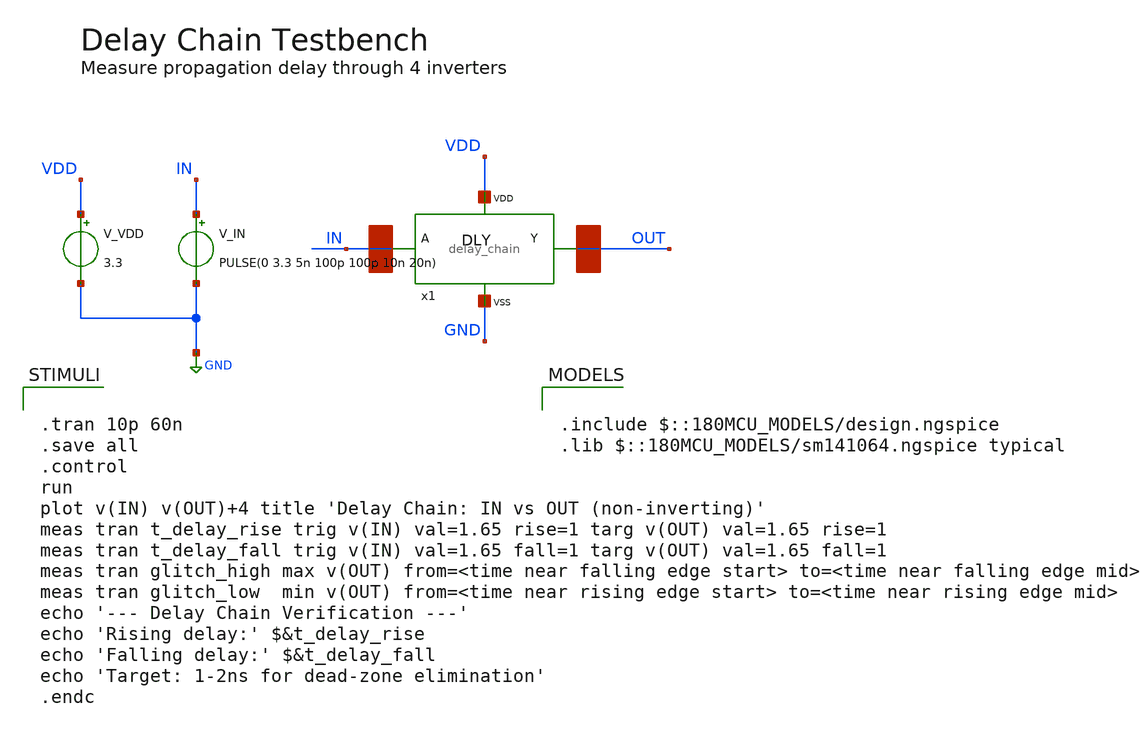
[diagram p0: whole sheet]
** sch_path: designs/libs/PDF/delay_chain_tb.sch
**.subckt delay_chain_tb
x1 IN OUT VDD GND delay_chain
V_IN IN GND PULSE(0 3.3 5n 100p 100p 10n 20n)
V_VDD VDD GND 3.3
**** begin user architecture code


.tran 10p 60n
.save all
.control
run
plot v(IN) v(OUT)+4 title 'Delay Chain: IN vs OUT (non-inverting)'
meas tran t_delay_rise trig v(IN) val=1.65 rise=1 targ v(OUT) val=1.65 rise=1
meas tran t_delay_fall trig v(IN) val=1.65 fall=1 targ v(OUT) val=1.65 fall=1
meas tran glitch_high max v(OUT) from=<time near falling edge start> to=<time near falling edge mid>
meas tran glitch_low  min v(OUT) from=<time near rising edge start> to=<time near rising edge mid>
echo '--- Delay Chain Verification ---'
echo 'Rising delay:' $&t_delay_rise
echo 'Falling delay:' $&t_delay_fall
echo 'Target: 1-2ns for dead-zone elimination'
.endc



.include $::180MCU_MODELS/design.ngspice
.lib $::180MCU_MODELS/sm141064.ngspice typical

**** end user architecture code
**.ends
.GLOBAL GND
.end
